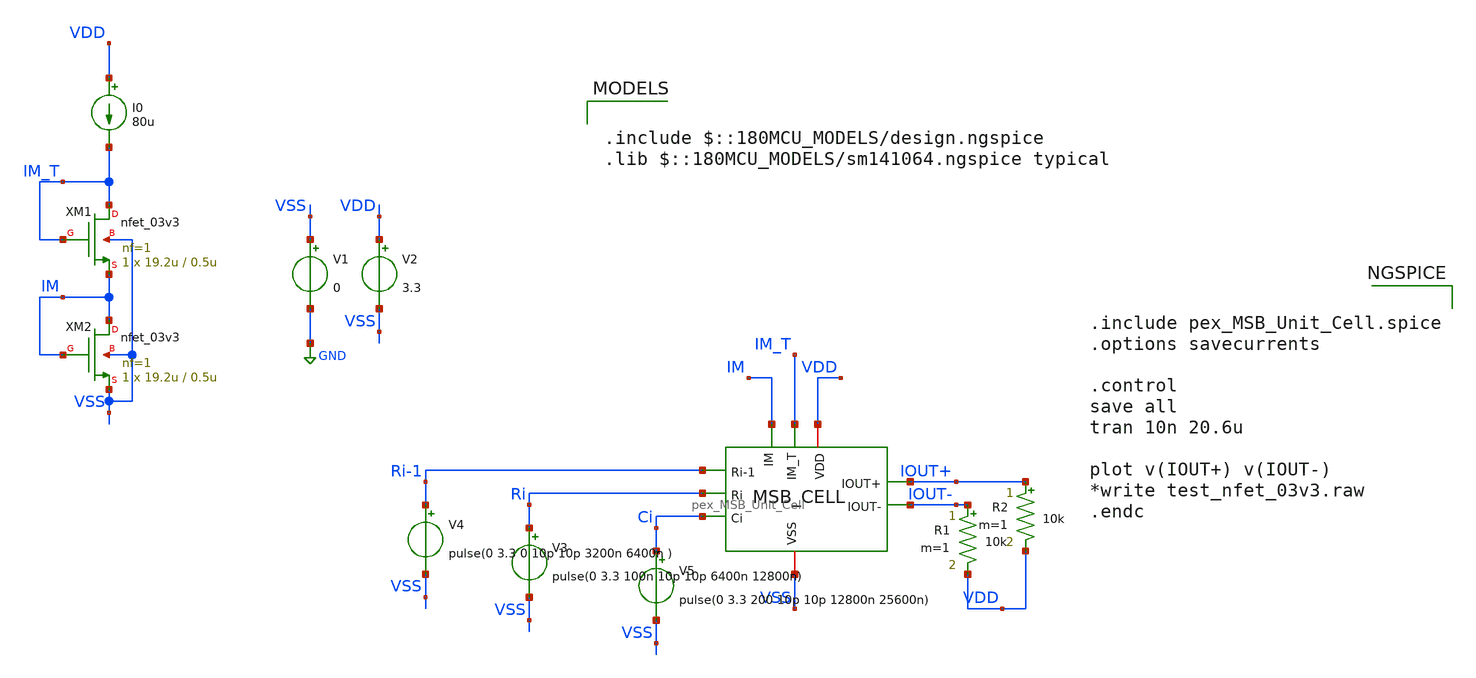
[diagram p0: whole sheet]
** sch_path: DAC_PAKISTAN_01/Pakistan1_Xschem/MSB_CELL_TB.sch
**.subckt MSB_CELL_TB
V1 VSS GND 0
V2 VDD VSS 3.3
I0 VDD IM_T 80u
XM1 IM_T IM_T IM VSS nfet_03v3 L=0.5u W=19.2u nf=1 ad='int((nf+1)/2) * W/nf * 0.18u' as='int((nf+2)/2) * W/nf * 0.18u'
+ pd='2*int((nf+1)/2) * (W/nf + 0.18u)' ps='2*int((nf+2)/2) * (W/nf + 0.18u)' nrd='0.18u / W' nrs='0.18u / W'
+ sa=0 sb=0 sd=0 m=1
XM2 IM IM VSS VSS nfet_03v3 L=0.5u W=19.2u nf=1 ad='int((nf+1)/2) * W/nf * 0.18u' as='int((nf+2)/2) * W/nf * 0.18u'
+ pd='2*int((nf+1)/2) * (W/nf + 0.18u)' ps='2*int((nf+2)/2) * (W/nf + 0.18u)' nrd='0.18u / W' nrs='0.18u / W'
+ sa=0 sb=0 sd=0 m=1
V4 Ri-1 VSS pulse(0 3.3 0 10p 10p 3200n 6400n )
V3 Ri VSS pulse(0 3.3 100n 10p 10p 6400n 12800n)
V5 Ci VSS pulse(0 3.3 200 10p 10p 12800n 25600n)
R1 IOUT- VDD 10k m=1
R2 IOUT+ VDD 10k m=1
x1 IOUT+ IOUT- VDD Ri-1 Ri Ci IM_T IM VSS pex_MSB_Unit_Cell
**** begin user architecture code

.include $::180MCU_MODELS/design.ngspice
.lib $::180MCU_MODELS/sm141064.ngspice typical



.include pex_MSB_Unit_Cell.spice
.options savecurrents

.control
save all
tran 10n 20.6u

plot v(IOUT+) v(IOUT-)
*write test_nfet_03v3.raw
.endc


**** end user architecture code
**.ends
.GLOBAL GND
.end
